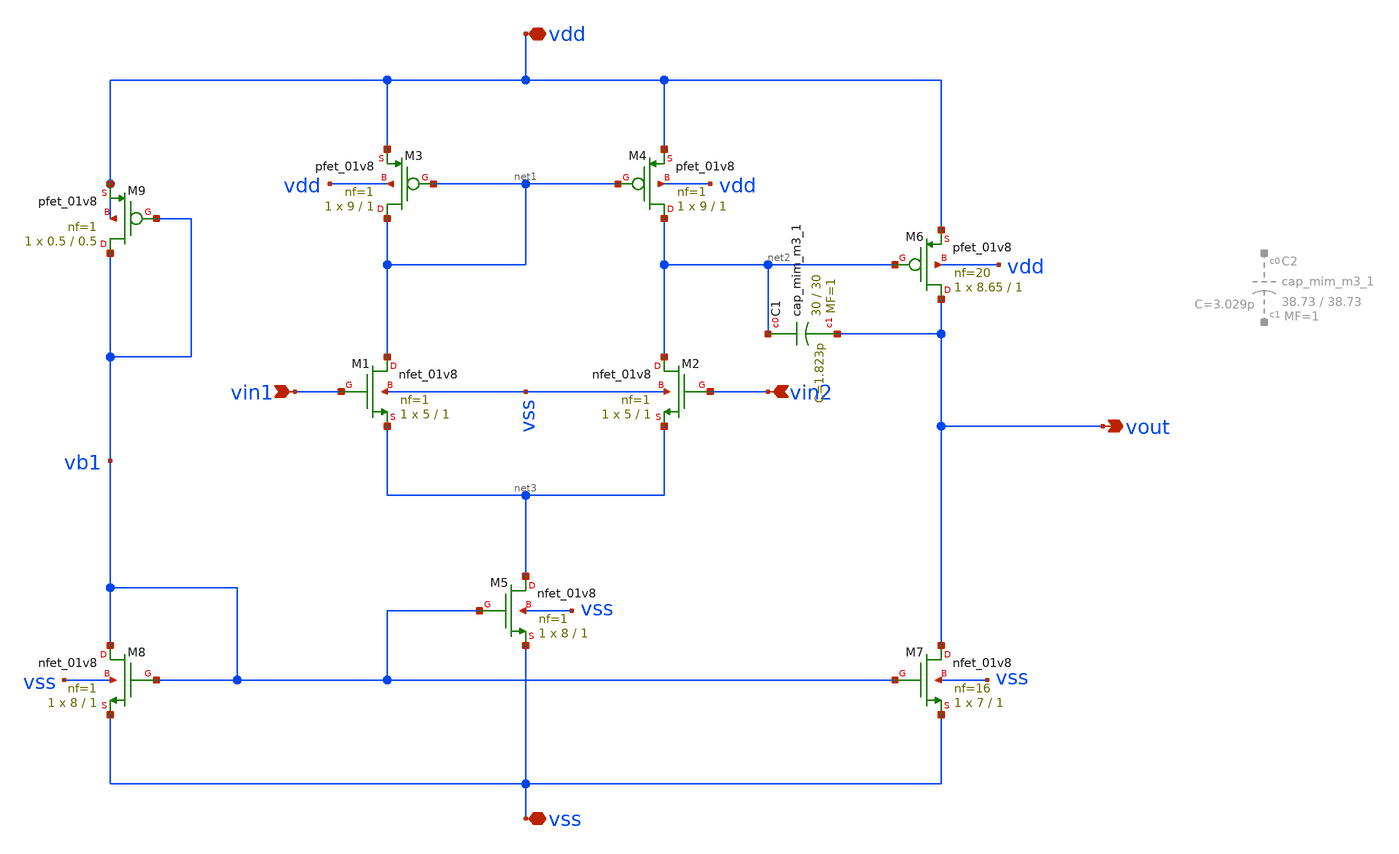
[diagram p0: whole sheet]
** sch_path: designs/libs/crossmem_ipn/opamp/opamp.sch
**.subckt opamp vss vdd vout vin1 vin2
*.iopin vss
*.iopin vdd
*.opin vout
*.ipin vin1
*.ipin vin2
XM3 net1 net1 vdd vdd sky130_fd_pr__pfet_01v8 L=1 W=9 nf=1 ad='int((1 + 1)/2) * 9 / 1 * 0.29' as='int((1 + 2)/2) * 9 / 1 * 0.29'
+ pd='2*int((1 + 1)/2) * (9 / 1 + 0.29)' ps='2*int((1 + 2)/2) * (9 / 1 + 0.29)' nrd='0.29 / 9 ' nrs='0.29 / 9 '
+ sa=0 sb=0 sd=0 mult=1 m=1
XM4 net2 net1 vdd vdd sky130_fd_pr__pfet_01v8 L=1 W=9 nf=1 ad='int((1 + 1)/2) * 9 / 1 * 0.29' as='int((1 + 2)/2) * 9 / 1 * 0.29'
+ pd='2*int((1 + 1)/2) * (9 / 1 + 0.29)' ps='2*int((1 + 2)/2) * (9 / 1 + 0.29)' nrd='0.29 / 9 ' nrs='0.29 / 9 '
+ sa=0 sb=0 sd=0 mult=1 m=1
XM6 vout net2 vdd vdd sky130_fd_pr__pfet_01v8 L=1 W=8.65 nf=20 ad='int((20 + 1)/2) * 8.65 / 20 * 0.29'
+ as='int((20 + 2)/2) * 8.65 / 20 * 0.29' pd='2*int((20 + 1)/2) * (8.65 / 20 + 0.29)' ps='2*int((20 + 2)/2) * (8.65 / 20 + 0.29)'
+ nrd='0.29 / 8.65 ' nrs='0.29 / 8.65 ' sa=0 sb=0 sd=0 mult=1 m=1
XM1 net1 vin1 net3 vss sky130_fd_pr__nfet_01v8 L=1 W=5 nf=1 ad='int((1 + 1)/2) * 5 / 1 * 0.29' as='int((1 + 2)/2) * 5 / 1 * 0.29'
+ pd='2*int((1 + 1)/2) * (5 / 1 + 0.29)' ps='2*int((1 + 2)/2) * (5 / 1 + 0.29)' nrd='0.29 / 5 ' nrs='0.29 / 5 '
+ sa=0 sb=0 sd=0 mult=1 m=1
XM2 net2 vin2 net3 vss sky130_fd_pr__nfet_01v8 L=1 W=5 nf=1 ad='int((1 + 1)/2) * 5 / 1 * 0.29' as='int((1 + 2)/2) * 5 / 1 * 0.29'
+ pd='2*int((1 + 1)/2) * (5 / 1 + 0.29)' ps='2*int((1 + 2)/2) * (5 / 1 + 0.29)' nrd='0.29 / 5 ' nrs='0.29 / 5 '
+ sa=0 sb=0 sd=0 mult=1 m=1
XM5 net3 vb1 vss vss sky130_fd_pr__nfet_01v8 L=1 W=8 nf=1 ad='int((1 + 1)/2) * 8 / 1 * 0.29' as='int((1 + 2)/2) * 8 / 1 * 0.29'
+ pd='2*int((1 + 1)/2) * (8 / 1 + 0.29)' ps='2*int((1 + 2)/2) * (8 / 1 + 0.29)' nrd='0.29 / 8 ' nrs='0.29 / 8 '
+ sa=0 sb=0 sd=0 mult=1 m=1
XM8 vb1 vb1 vss vss sky130_fd_pr__nfet_01v8 L=1 W=8 nf=1 ad='int((1 + 1)/2) * 8 / 1 * 0.29' as='int((1 + 2)/2) * 8 / 1 * 0.29'
+ pd='2*int((1 + 1)/2) * (8 / 1 + 0.29)' ps='2*int((1 + 2)/2) * (8 / 1 + 0.29)' nrd='0.29 / 8 ' nrs='0.29 / 8 '
+ sa=0 sb=0 sd=0 mult=1 m=1
XM7 vout vb1 vss vss sky130_fd_pr__nfet_01v8 L=1 W=7 nf=16 ad='int((16 + 1)/2) * 7 / 16 * 0.29' as='int((16 + 2)/2) * 7 / 16 * 0.29'
+ pd='2*int((16 + 1)/2) * (7 / 16 + 0.29)' ps='2*int((16 + 2)/2) * (7 / 16 + 0.29)' nrd='0.29 / 7 ' nrs='0.29 / 7 '
+ sa=0 sb=0 sd=0 mult=1 m=1
XC1 net2 vout sky130_fd_pr__cap_mim_m3_1 W=30 L=30 MF=1 m=1
XM9 vb1 vb1 vdd vdd sky130_fd_pr__pfet_01v8 L=0.5 W=0.5 nf=1 ad='int((1 + 1)/2) * 0.5 / 1 * 0.29' as='int((1 + 2)/2) * 0.5 / 1 * 0.29'
+ pd='2*int((1 + 1)/2) * (0.5 / 1 + 0.29)' ps='2*int((1 + 2)/2) * (0.5 / 1 + 0.29)' nrd='0.29 / 0.5 ' nrs='0.29 / 0.5 '
+ sa=0 sb=0 sd=0 mult=1 m=1
**.ends
.end
